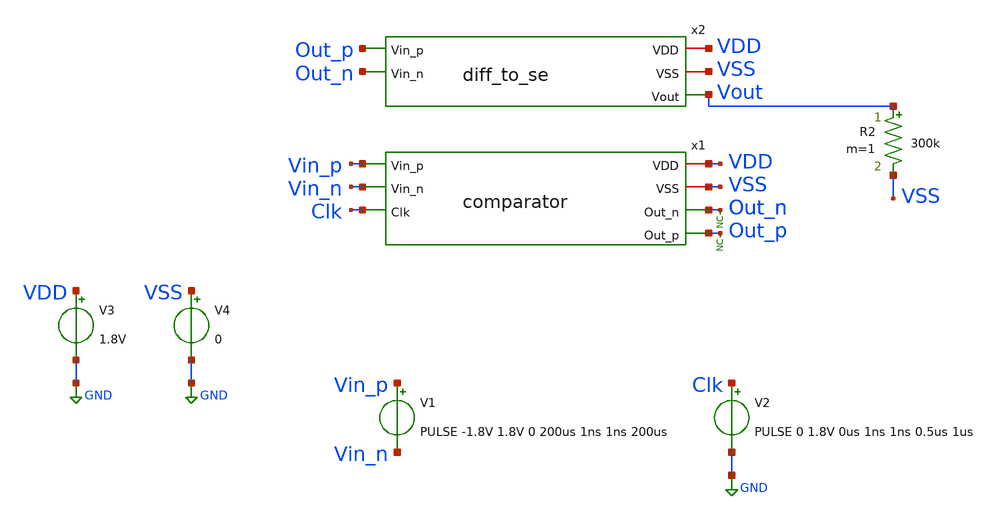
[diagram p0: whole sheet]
** sch_path: xschem/tests/diff_to_se/diff_to_se_test.sch
**.subckt diff_to_se_test
V3 VDD GND 1.8V
V4 VSS GND 0
x1 VDD VSS Vin_p Out_n Vin_n Out_p Clk comparator
V1 Vin_p Vin_n PULSE -1.8V 1.8V 0 200us 1ns 1ns 200us
V2 Clk GND PULSE 0 1.8V 0us 1ns 1ns 0.5us 1us
* noconn Out_p
* noconn Out_n
x2 VDD VSS Out_p Out_n Vout diff_to_se
R2 Vout VSS 300k m=1
**** begin user architecture code
 .lib $::SKYWATER_MODELS/sky130.lib.spice tt
.include $::SKYWATER_STDCELLS/sky130_fd_sc_hd.spice


.options acct list
.temp 25
*vvcc VDD 0 dc 1.8
*vvss VSS 0 0
.control
tran 0.1u 200u
*dc V1 0 1.8V 0.1
plot Vin_p-Vin_n Out_p-Out_n Clk-4
plot out_p-out_n Vout+2
write comparator_test.raw
.endc


**** end user architecture code
**.ends

* expanding   symbol:  src/comparator/comparator.sym # of pins=7
** sym_path: xschem/src/comparator/comparator.sym
** sch_path: xschem/src/comparator/comparator.sch
.subckt comparator VDD VSS Vin_p Out_n Vin_n Out_p Clk
*.iopin VDD
*.iopin VSS
*.ipin Vin_p
*.opin Out_n
*.ipin Vin_n
*.opin Out_p
*.ipin Clk
XM1 Pre_Amp_n Clk VDD VSS sky130_fd_pr__pfet_01v8 L=0.15 W=1 nf=1 ad='int((nf+1)/2) * W/nf * 0.29' as='int((nf+2)/2) * W/nf * 0.29'
+ pd='2*int((nf+1)/2) * (W/nf + 0.29)' ps='2*int((nf+2)/2) * (W/nf + 0.29)' nrd='0.29 / W' nrs='0.29 / W'
+ sa=0 sb=0 sd=0 mult=1 m=1
XM2 Pre_Amp_p Clk VDD VSS sky130_fd_pr__pfet_01v8 L=0.15 W=1 nf=1 ad='int((nf+1)/2) * W/nf * 0.29' as='int((nf+2)/2) * W/nf * 0.29'
+ pd='2*int((nf+1)/2) * (W/nf + 0.29)' ps='2*int((nf+2)/2) * (W/nf + 0.29)' nrd='0.29 / W' nrs='0.29 / W'
+ sa=0 sb=0 sd=0 mult=1 m=1
XM3 Pre_Amp_p Vin_p net1 VSS sky130_fd_pr__nfet_01v8 L=0.15 W=1 nf=1 ad='int((nf+1)/2) * W/nf * 0.29'
+ as='int((nf+2)/2) * W/nf * 0.29' pd='2*int((nf+1)/2) * (W/nf + 0.29)' ps='2*int((nf+2)/2) * (W/nf + 0.29)'
+ nrd='0.29 / W' nrs='0.29 / W' sa=0 sb=0 sd=0 mult=1 m=1
XM4 Pre_Amp_n Vin_n net1 VSS sky130_fd_pr__nfet_01v8 L=0.15 W=1 nf=1 ad='int((nf+1)/2) * W/nf * 0.29'
+ as='int((nf+2)/2) * W/nf * 0.29' pd='2*int((nf+1)/2) * (W/nf + 0.29)' ps='2*int((nf+2)/2) * (W/nf + 0.29)'
+ nrd='0.29 / W' nrs='0.29 / W' sa=0 sb=0 sd=0 mult=1 m=1
XM5 net3 Out_p VDD VSS sky130_fd_pr__pfet_01v8 L=0.15 W=1 nf=1 ad='int((nf+1)/2) * W/nf * 0.29' as='int((nf+2)/2) * W/nf * 0.29'
+ pd='2*int((nf+1)/2) * (W/nf + 0.29)' ps='2*int((nf+2)/2) * (W/nf + 0.29)' nrd='0.29 / W' nrs='0.29 / W'
+ sa=0 sb=0 sd=0 mult=1 m=1
XM6 net2 Out_n VDD VSS sky130_fd_pr__pfet_01v8 L=0.15 W=1 nf=1 ad='int((nf+1)/2) * W/nf * 0.29' as='int((nf+2)/2) * W/nf * 0.29'
+ pd='2*int((nf+1)/2) * (W/nf + 0.29)' ps='2*int((nf+2)/2) * (W/nf + 0.29)' nrd='0.29 / W' nrs='0.29 / W'
+ sa=0 sb=0 sd=0 mult=1 m=1
XM7 net2 Pre_Amp_p Out_p VSS sky130_fd_pr__nfet_01v8 L=0.15 W=1 nf=1 ad='int((nf+1)/2) * W/nf * 0.29'
+ as='int((nf+2)/2) * W/nf * 0.29' pd='2*int((nf+1)/2) * (W/nf + 0.29)' ps='2*int((nf+2)/2) * (W/nf + 0.29)'
+ nrd='0.29 / W' nrs='0.29 / W' sa=0 sb=0 sd=0 mult=1 m=1
XM8 net3 Pre_Amp_n Out_n VSS sky130_fd_pr__nfet_01v8 L=0.15 W=1 nf=1 ad='int((nf+1)/2) * W/nf * 0.29'
+ as='int((nf+2)/2) * W/nf * 0.29' pd='2*int((nf+1)/2) * (W/nf + 0.29)' ps='2*int((nf+2)/2) * (W/nf + 0.29)'
+ nrd='0.29 / W' nrs='0.29 / W' sa=0 sb=0 sd=0 mult=1 m=1
XM9 net1 Clk VSS VSS sky130_fd_pr__nfet_01v8 L=0.15 W=1 nf=1 ad='int((nf+1)/2) * W/nf * 0.29' as='int((nf+2)/2) * W/nf * 0.29'
+ pd='2*int((nf+1)/2) * (W/nf + 0.29)' ps='2*int((nf+2)/2) * (W/nf + 0.29)' nrd='0.29 / W' nrs='0.29 / W'
+ sa=0 sb=0 sd=0 mult=1 m=1
XM10 Pre_Amp_n Vin_n net1 VSS sky130_fd_pr__nfet_01v8 L=0.15 W=1 nf=1 ad='int((nf+1)/2) * W/nf * 0.29'
+ as='int((nf+2)/2) * W/nf * 0.29' pd='2*int((nf+1)/2) * (W/nf + 0.29)' ps='2*int((nf+2)/2) * (W/nf + 0.29)'
+ nrd='0.29 / W' nrs='0.29 / W' sa=0 sb=0 sd=0 mult=1 m=1
XM11 Out_n Clk_n VSS VSS sky130_fd_pr__nfet_01v8 L=0.15 W=1 nf=1 ad='int((nf+1)/2) * W/nf * 0.29' as='int((nf+2)/2) * W/nf * 0.29'
+ pd='2*int((nf+1)/2) * (W/nf + 0.29)' ps='2*int((nf+2)/2) * (W/nf + 0.29)' nrd='0.29 / W' nrs='0.29 / W'
+ sa=0 sb=0 sd=0 mult=1 m=1
XM12 Out_n Out_p VSS VSS sky130_fd_pr__nfet_01v8 L=0.15 W=1 nf=1 ad='int((nf+1)/2) * W/nf * 0.29' as='int((nf+2)/2) * W/nf * 0.29'
+ pd='2*int((nf+1)/2) * (W/nf + 0.29)' ps='2*int((nf+2)/2) * (W/nf + 0.29)' nrd='0.29 / W' nrs='0.29 / W'
+ sa=0 sb=0 sd=0 mult=1 m=1
XM13 Out_p Out_n VSS VSS sky130_fd_pr__nfet_01v8 L=0.15 W=1 nf=1 ad='int((nf+1)/2) * W/nf * 0.29' as='int((nf+2)/2) * W/nf * 0.29'
+ pd='2*int((nf+1)/2) * (W/nf + 0.29)' ps='2*int((nf+2)/2) * (W/nf + 0.29)' nrd='0.29 / W' nrs='0.29 / W'
+ sa=0 sb=0 sd=0 mult=1 m=1
XM14 Out_p Clk_n VSS VSS sky130_fd_pr__nfet_01v8 L=0.15 W=1 nf=1 ad='int((nf+1)/2) * W/nf * 0.29' as='int((nf+2)/2) * W/nf * 0.29'
+ pd='2*int((nf+1)/2) * (W/nf + 0.29)' ps='2*int((nf+2)/2) * (W/nf + 0.29)' nrd='0.29 / W' nrs='0.29 / W'
+ sa=0 sb=0 sd=0 mult=1 m=1
XM15 Clk_n Clk VDD VSS sky130_fd_pr__pfet_01v8 L=0.15 W=1 nf=1 ad='int((nf+1)/2) * W/nf * 0.29' as='int((nf+2)/2) * W/nf * 0.29'
+ pd='2*int((nf+1)/2) * (W/nf + 0.29)' ps='2*int((nf+2)/2) * (W/nf + 0.29)' nrd='0.29 / W' nrs='0.29 / W'
+ sa=0 sb=0 sd=0 mult=1 m=1
XM16 Clk_n Clk VSS VSS sky130_fd_pr__nfet_01v8 L=0.15 W=1 nf=1 ad='int((nf+1)/2) * W/nf * 0.29' as='int((nf+2)/2) * W/nf * 0.29'
+ pd='2*int((nf+1)/2) * (W/nf + 0.29)' ps='2*int((nf+2)/2) * (W/nf + 0.29)' nrd='0.29 / W' nrs='0.29 / W'
+ sa=0 sb=0 sd=0 mult=1 m=1
.ends


* expanding   symbol:  src/diff_to_se/diff_to_se.sym # of pins=5
** sym_path: xschem/src/diff_to_se/diff_to_se.sym
** sch_path: xschem/src/diff_to_se/diff_to_se.sch
.subckt diff_to_se VDD VSS Vin_p Vin_n Vout
*.iopin VDD
*.opin Vout
*.ipin Vin_p
*.ipin Vin_n
*.iopin VSS
XM1 net4 Vin_p net2 VSS sky130_fd_pr__nfet_01v8 L=0.15 W=3.75 nf=1 ad='int((nf+1)/2) * W/nf * 0.29' as='int((nf+2)/2) * W/nf * 0.29'
+ pd='2*int((nf+1)/2) * (W/nf + 0.29)' ps='2*int((nf+2)/2) * (W/nf + 0.29)' nrd='0.29 / W' nrs='0.29 / W'
+ sa=0 sb=0 sd=0 mult=1 m=1
XM2 Vout net1 VDD VDD sky130_fd_pr__pfet_01v8 L=0.15 W=6.62 nf=1 ad='int((nf+1)/2) * W/nf * 0.29' as='int((nf+2)/2) * W/nf * 0.29'
+ pd='2*int((nf+1)/2) * (W/nf + 0.29)' ps='2*int((nf+2)/2) * (W/nf + 0.29)' nrd='0.29 / W' nrs='0.29 / W'
+ sa=0 sb=0 sd=0 mult=1 m=1
XM3 net1 net1 VDD VDD sky130_fd_pr__pfet_01v8 L=0.15 W=6.62 nf=1 ad='int((nf+1)/2) * W/nf * 0.29' as='int((nf+2)/2) * W/nf * 0.29'
+ pd='2*int((nf+1)/2) * (W/nf + 0.29)' ps='2*int((nf+2)/2) * (W/nf + 0.29)' nrd='0.29 / W' nrs='0.29 / W'
+ sa=0 sb=0 sd=0 mult=1 m=1
XM4 net5 Vin_n net2 VSS sky130_fd_pr__nfet_01v8 L=0.15 W=3.75 nf=1 ad='int((nf+1)/2) * W/nf * 0.29' as='int((nf+2)/2) * W/nf * 0.29'
+ pd='2*int((nf+1)/2) * (W/nf + 0.29)' ps='2*int((nf+2)/2) * (W/nf + 0.29)' nrd='0.29 / W' nrs='0.29 / W'
+ sa=0 sb=0 sd=0 mult=1 m=1
XM5 net3 VDD VSS VSS sky130_fd_pr__nfet_01v8 L=0.15 W=3.75 nf=1 ad='int((nf+1)/2) * W/nf * 0.29' as='int((nf+2)/2) * W/nf * 0.29'
+ pd='2*int((nf+1)/2) * (W/nf + 0.29)' ps='2*int((nf+2)/2) * (W/nf + 0.29)' nrd='0.29 / W' nrs='0.29 / W'
+ sa=0 sb=0 sd=0 mult=10 m=10
V1 net2 net3 0
V2 Vout net5 0
V3 net1 net4 0
.ends

.GLOBAL GND
.end
